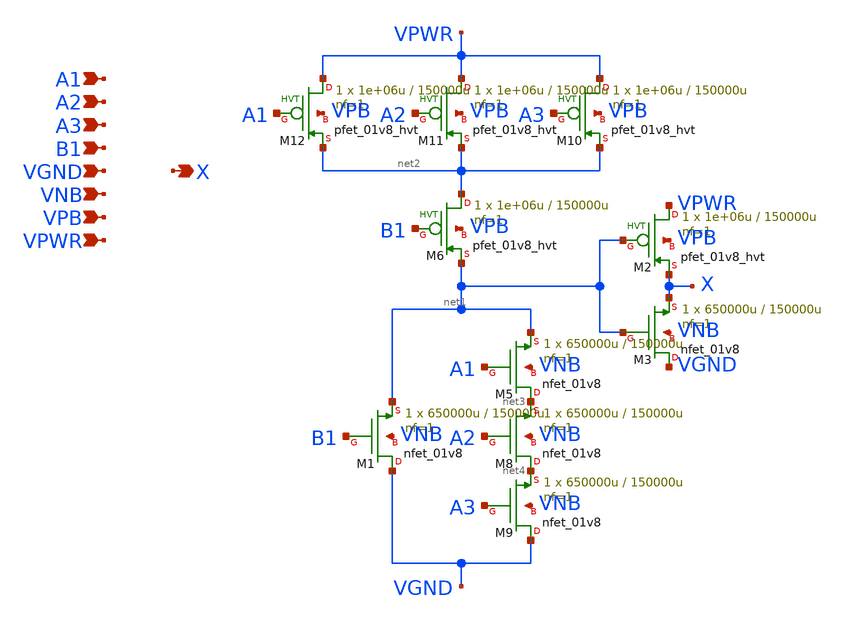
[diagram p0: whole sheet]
** sch_path: schematics/a31o/sky130_fd_sc_hd__a31o_1.sch
**.subckt sky130_fd_sc_hd__a31o_1 A3 X B1 VGND VNB VPB VPWR A2 A1
*.ipin A3
*.opin X
*.ipin B1
*.ipin VGND
*.ipin VNB
*.ipin VPB
*.ipin VPWR
*.ipin A2
*.ipin A1
XM1 VGND B1 net1 VNB sky130_fd_pr__nfet_01v8 L=150000u W=650000u nf=1 ad='int((1 + 1)/2) * 650000u / 1 * 0.29'
+ as='int((1 + 2)/2) * 650000u / 1 * 0.29' pd='2*int((1 + 1)/2) * (650000u / 1 + 0.29)' ps='2*int((1 + 2)/2) * (650000u / 1 + 0.29)'
+ nrd='0.29 / 650000u ' nrs='0.29 / 650000u ' sa=0 sb=0 sd=0 mult=1 m=1
XM2 VPWR net1 X VPB sky130_fd_pr__pfet_01v8_hvt L=150000u W=1e+06u nf=1 ad='int((1 + 1)/2) * 1e+06u / 1 * 0.29'
+ as='int((1 + 2)/2) * 1e+06u / 1 * 0.29' pd='2*int((1 + 1)/2) * (1e+06u / 1 + 0.29)' ps='2*int((1 + 2)/2) * (1e+06u / 1 + 0.29)'
+ nrd='0.29 / 1e+06u ' nrs='0.29 / 1e+06u ' sa=0 sb=0 sd=0 mult=1 m=1
XM3 VGND net1 X VNB sky130_fd_pr__nfet_01v8 L=150000u W=650000u nf=1 ad='int((1 + 1)/2) * 650000u / 1 * 0.29'
+ as='int((1 + 2)/2) * 650000u / 1 * 0.29' pd='2*int((1 + 1)/2) * (650000u / 1 + 0.29)' ps='2*int((1 + 2)/2) * (650000u / 1 + 0.29)'
+ nrd='0.29 / 650000u ' nrs='0.29 / 650000u ' sa=0 sb=0 sd=0 mult=1 m=1
XM5 net3 A1 net1 VNB sky130_fd_pr__nfet_01v8 L=150000u W=650000u nf=1 ad='int((1 + 1)/2) * 650000u / 1 * 0.29'
+ as='int((1 + 2)/2) * 650000u / 1 * 0.29' pd='2*int((1 + 1)/2) * (650000u / 1 + 0.29)' ps='2*int((1 + 2)/2) * (650000u / 1 + 0.29)'
+ nrd='0.29 / 650000u ' nrs='0.29 / 650000u ' sa=0 sb=0 sd=0 mult=1 m=1
XM6 net2 B1 net1 VPB sky130_fd_pr__pfet_01v8_hvt L=150000u W=1e+06u nf=1 ad='int((1 + 1)/2) * 1e+06u / 1 * 0.29'
+ as='int((1 + 2)/2) * 1e+06u / 1 * 0.29' pd='2*int((1 + 1)/2) * (1e+06u / 1 + 0.29)' ps='2*int((1 + 2)/2) * (1e+06u / 1 + 0.29)'
+ nrd='0.29 / 1e+06u ' nrs='0.29 / 1e+06u ' sa=0 sb=0 sd=0 mult=1 m=1
XM8 net4 A2 net3 VNB sky130_fd_pr__nfet_01v8 L=150000u W=650000u nf=1 ad='int((1 + 1)/2) * 650000u / 1 * 0.29'
+ as='int((1 + 2)/2) * 650000u / 1 * 0.29' pd='2*int((1 + 1)/2) * (650000u / 1 + 0.29)' ps='2*int((1 + 2)/2) * (650000u / 1 + 0.29)'
+ nrd='0.29 / 650000u ' nrs='0.29 / 650000u ' sa=0 sb=0 sd=0 mult=1 m=1
XM9 VGND A3 net4 VNB sky130_fd_pr__nfet_01v8 L=150000u W=650000u nf=1 ad='int((1 + 1)/2) * 650000u / 1 * 0.29'
+ as='int((1 + 2)/2) * 650000u / 1 * 0.29' pd='2*int((1 + 1)/2) * (650000u / 1 + 0.29)' ps='2*int((1 + 2)/2) * (650000u / 1 + 0.29)'
+ nrd='0.29 / 650000u ' nrs='0.29 / 650000u ' sa=0 sb=0 sd=0 mult=1 m=1
XM10 VPWR A3 net2 VPB sky130_fd_pr__pfet_01v8_hvt L=150000u W=1e+06u nf=1 ad='int((1 + 1)/2) * 1e+06u / 1 * 0.29'
+ as='int((1 + 2)/2) * 1e+06u / 1 * 0.29' pd='2*int((1 + 1)/2) * (1e+06u / 1 + 0.29)' ps='2*int((1 + 2)/2) * (1e+06u / 1 + 0.29)'
+ nrd='0.29 / 1e+06u ' nrs='0.29 / 1e+06u ' sa=0 sb=0 sd=0 mult=1 m=1
XM11 VPWR A2 net2 VPB sky130_fd_pr__pfet_01v8_hvt L=150000u W=1e+06u nf=1 ad='int((1 + 1)/2) * 1e+06u / 1 * 0.29'
+ as='int((1 + 2)/2) * 1e+06u / 1 * 0.29' pd='2*int((1 + 1)/2) * (1e+06u / 1 + 0.29)' ps='2*int((1 + 2)/2) * (1e+06u / 1 + 0.29)'
+ nrd='0.29 / 1e+06u ' nrs='0.29 / 1e+06u ' sa=0 sb=0 sd=0 mult=1 m=1
XM12 VPWR A1 net2 VPB sky130_fd_pr__pfet_01v8_hvt L=150000u W=1e+06u nf=1 ad='int((1 + 1)/2) * 1e+06u / 1 * 0.29'
+ as='int((1 + 2)/2) * 1e+06u / 1 * 0.29' pd='2*int((1 + 1)/2) * (1e+06u / 1 + 0.29)' ps='2*int((1 + 2)/2) * (1e+06u / 1 + 0.29)'
+ nrd='0.29 / 1e+06u ' nrs='0.29 / 1e+06u ' sa=0 sb=0 sd=0 mult=1 m=1
**.ends
.end
